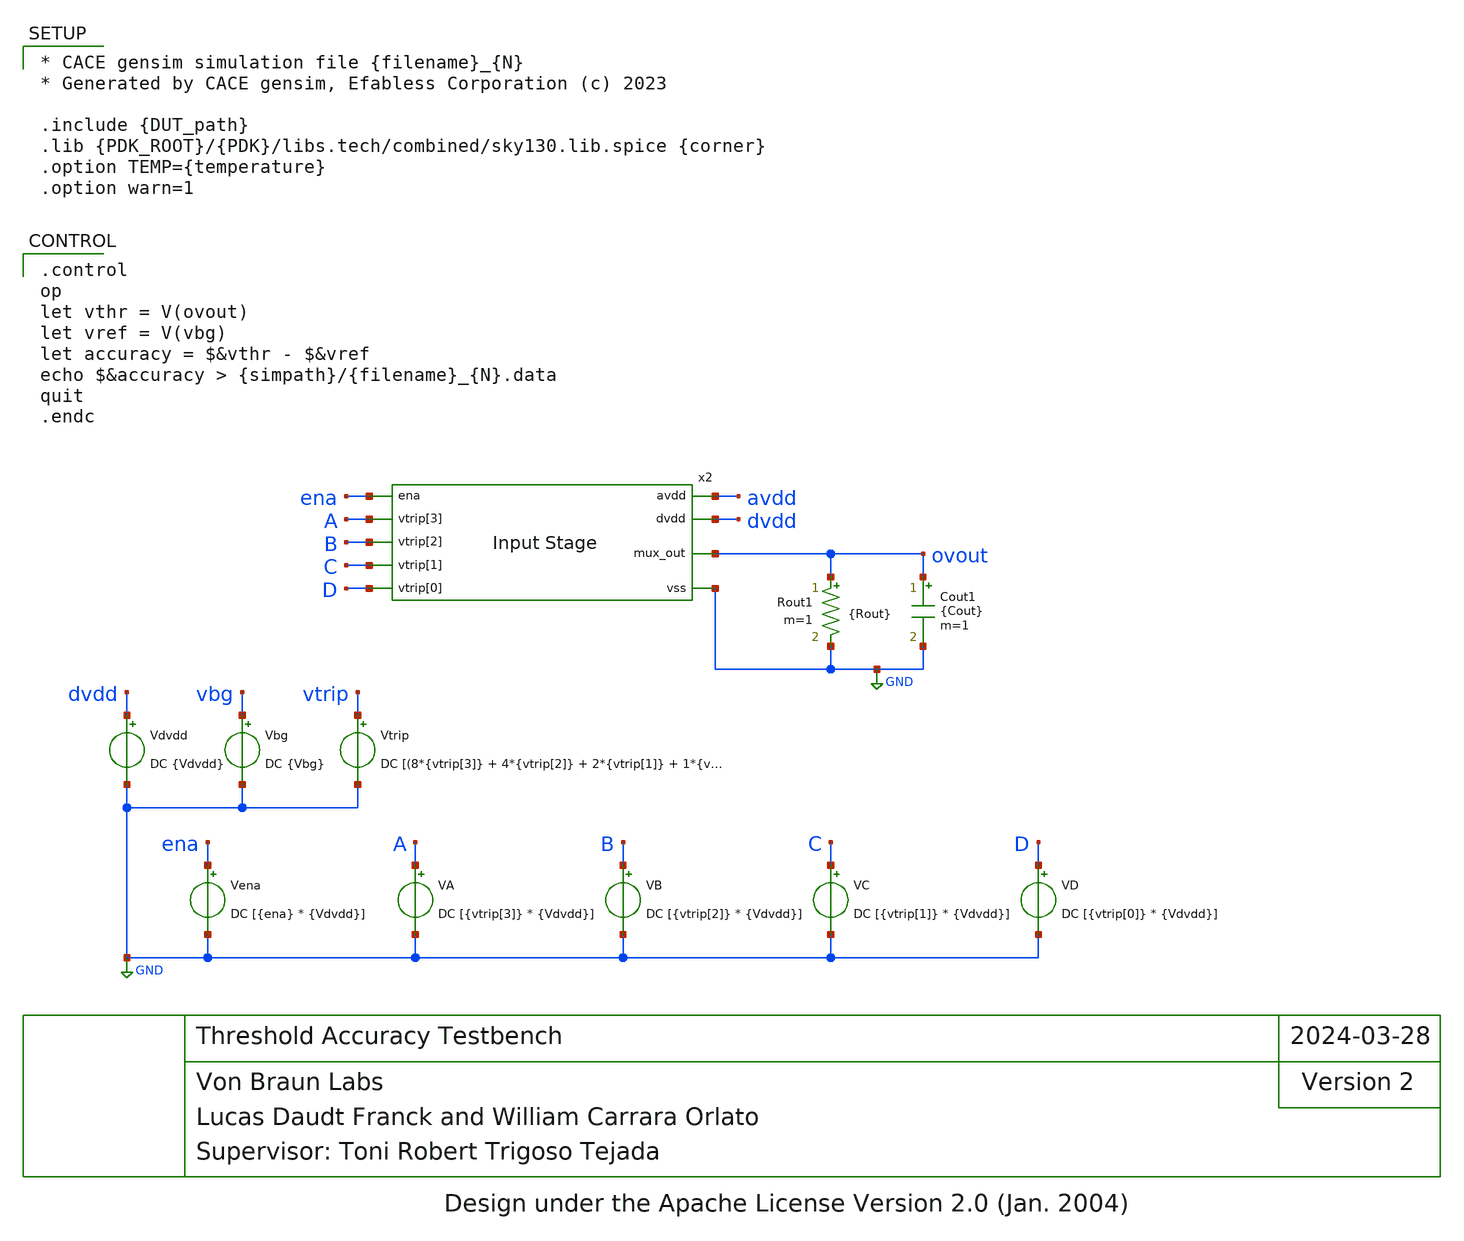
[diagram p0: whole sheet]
** sch_path: blocks/input/cace/tb_vacc.sch
* Design under the Apache License Version 2.0 (Jan. 2004)
**.subckt tb_vacc
Vdvdd dvdd GND DC {Vdvdd}
Vbg vbg GND DC {Vbg}
Vena ena GND DC [{ena} * {Vdvdd}]
VA A GND DC [{vtrip[3]} * {Vdvdd}]
VB B GND DC [{vtrip[2]} * {Vdvdd}]
VC C GND DC [{vtrip[1]} * {Vdvdd}]
VD D GND DC [{vtrip[0]} * {Vdvdd}]
Vtrip vtrip GND DC [(8*{vtrip[3]} + 4*{vtrip[2]} + 2*{vtrip[1]} + 1*{vtrip[0]})*0.14667 + 3.3]
Cout1 ovout GND {Cout} m=1
Rout1 ovout GND {Rout} m=1
x2 avdd dvdd ena A GND B ovout C D input
**** begin user architecture code

* CACE gensim simulation file {filename}_{N}
* Generated by CACE gensim, Efabless Corporation (c) 2023

.include {DUT_path}
.lib {PDK_ROOT}/{PDK}/libs.tech/combined/sky130.lib.spice {corner}
.option TEMP={temperature}
.option warn=1



.control
op
let vthr = V(ovout)
let vref = V(vbg)
let accuracy = $&vthr - $&vref
echo $&accuracy > {simpath}/{filename}_{N}.data
quit
.endc


**** end user architecture code
**.ends
.GLOBAL GND
.end
